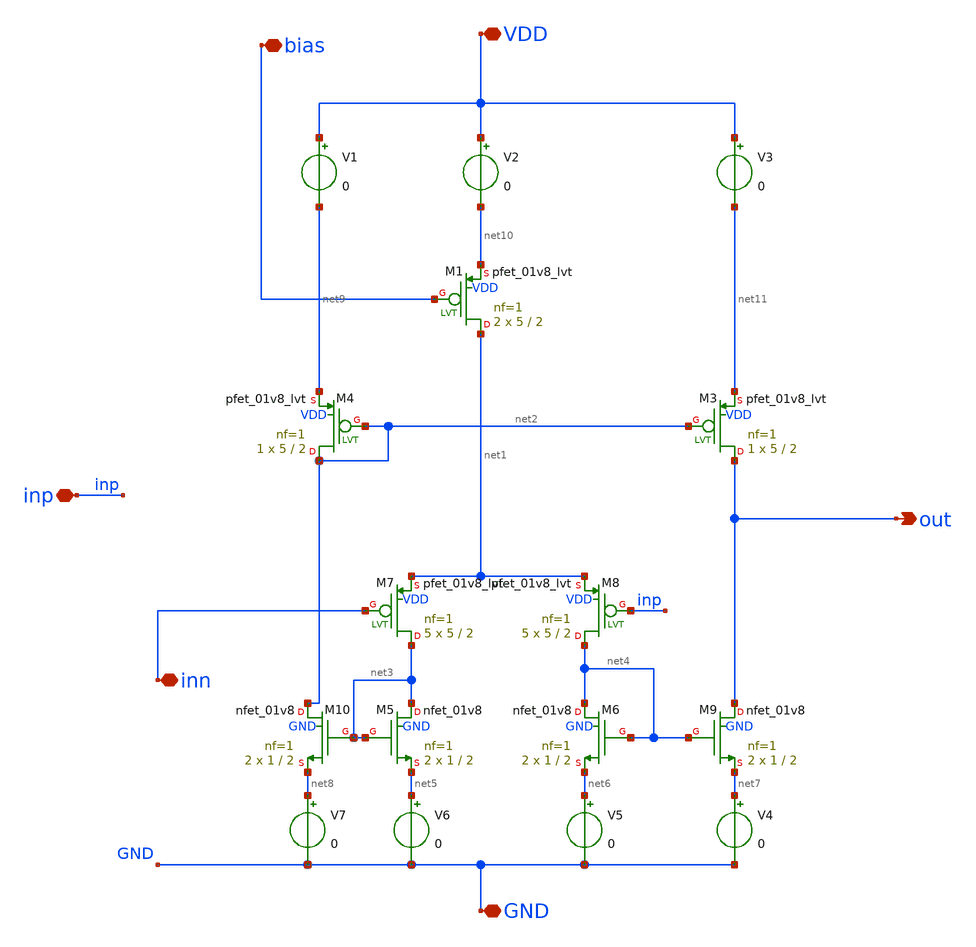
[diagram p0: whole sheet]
** sch_path: NES-2026/STDCELLS/xschem/opamp.sch
**.subckt opamp VDD GND out inn inp bias
*.iopin VDD
*.iopin GND
*.opin out
*.iopin inn
*.iopin inp
*.iopin bias
XM1 net1 bias net10 VDD sky130_fd_pr__pfet_01v8_lvt L=2 W=5 nf=1 ad='int((1 + 1)/2) * 5 / 1 * 0.29' as='int((1 + 2)/2) * 5 / 1 * 0.29'
+ pd='2*int((1 + 1)/2) * (5 / 1 + 0.29)' ps='2*int((1 + 2)/2) * (5 / 1 + 0.29)' nrd='0.29 / 5 ' nrs='0.29 / 5 '
+ sa=0 sb=0 sd=0 mult=2 m=2
XM3 out net2 net11 VDD sky130_fd_pr__pfet_01v8_lvt L=2 W=5 nf=1 ad='int((1 + 1)/2) * 5 / 1 * 0.29' as='int((1 + 2)/2) * 5 / 1 * 0.29'
+ pd='2*int((1 + 1)/2) * (5 / 1 + 0.29)' ps='2*int((1 + 2)/2) * (5 / 1 + 0.29)' nrd='0.29 / 5 ' nrs='0.29 / 5 '
+ sa=0 sb=0 sd=0 mult=1 m=1
XM4 net2 net2 net9 VDD sky130_fd_pr__pfet_01v8_lvt L=2 W=5 nf=1 ad='int((1 + 1)/2) * 5 / 1 * 0.29' as='int((1 + 2)/2) * 5 / 1 * 0.29'
+ pd='2*int((1 + 1)/2) * (5 / 1 + 0.29)' ps='2*int((1 + 2)/2) * (5 / 1 + 0.29)' nrd='0.29 / 5 ' nrs='0.29 / 5 '
+ sa=0 sb=0 sd=0 mult=1 m=1
XM5 net3 net3 net5 GND sky130_fd_pr__nfet_01v8 L=2 W=1 nf=1 ad='int((1 + 1)/2) * 1 / 1 * 0.29' as='int((1 + 2)/2) * 1 / 1 * 0.29'
+ pd='2*int((1 + 1)/2) * (1 / 1 + 0.29)' ps='2*int((1 + 2)/2) * (1 / 1 + 0.29)' nrd='0.29 / 1 ' nrs='0.29 / 1 '
+ sa=0 sb=0 sd=0 mult=2 m=2
XM6 net4 net4 net6 GND sky130_fd_pr__nfet_01v8 L=2 W=1 nf=1 ad='int((1 + 1)/2) * 1 / 1 * 0.29' as='int((1 + 2)/2) * 1 / 1 * 0.29'
+ pd='2*int((1 + 1)/2) * (1 / 1 + 0.29)' ps='2*int((1 + 2)/2) * (1 / 1 + 0.29)' nrd='0.29 / 1 ' nrs='0.29 / 1 '
+ sa=0 sb=0 sd=0 mult=2 m=2
XM7 net3 inn net1 VDD sky130_fd_pr__pfet_01v8_lvt L=2 W=5 nf=1 ad='int((1 + 1)/2) * 5 / 1 * 0.29' as='int((1 + 2)/2) * 5 / 1 * 0.29'
+ pd='2*int((1 + 1)/2) * (5 / 1 + 0.29)' ps='2*int((1 + 2)/2) * (5 / 1 + 0.29)' nrd='0.29 / 5 ' nrs='0.29 / 5 '
+ sa=0 sb=0 sd=0 mult=5 m=5
XM8 net4 inp net1 VDD sky130_fd_pr__pfet_01v8_lvt L=2 W=5 nf=1 ad='int((1 + 1)/2) * 5 / 1 * 0.29' as='int((1 + 2)/2) * 5 / 1 * 0.29'
+ pd='2*int((1 + 1)/2) * (5 / 1 + 0.29)' ps='2*int((1 + 2)/2) * (5 / 1 + 0.29)' nrd='0.29 / 5 ' nrs='0.29 / 5 '
+ sa=0 sb=0 sd=0 mult=5 m=5
XM9 out net4 net7 GND sky130_fd_pr__nfet_01v8 L=2 W=1 nf=1 ad='int((1 + 1)/2) * 1 / 1 * 0.29' as='int((1 + 2)/2) * 1 / 1 * 0.29'
+ pd='2*int((1 + 1)/2) * (1 / 1 + 0.29)' ps='2*int((1 + 2)/2) * (1 / 1 + 0.29)' nrd='0.29 / 1 ' nrs='0.29 / 1 '
+ sa=0 sb=0 sd=0 mult=2 m=2
XM10 net2 net3 net8 GND sky130_fd_pr__nfet_01v8 L=2 W=1 nf=1 ad='int((1 + 1)/2) * 1 / 1 * 0.29' as='int((1 + 2)/2) * 1 / 1 * 0.29'
+ pd='2*int((1 + 1)/2) * (1 / 1 + 0.29)' ps='2*int((1 + 2)/2) * (1 / 1 + 0.29)' nrd='0.29 / 1 ' nrs='0.29 / 1 '
+ sa=0 sb=0 sd=0 mult=2 m=2
V1 VDD net9 0
V2 VDD net10 0
V3 VDD net11 0
V4 net7 GND 0
V5 net6 GND 0
V6 net5 GND 0
V7 net8 GND 0
**.ends
.end
